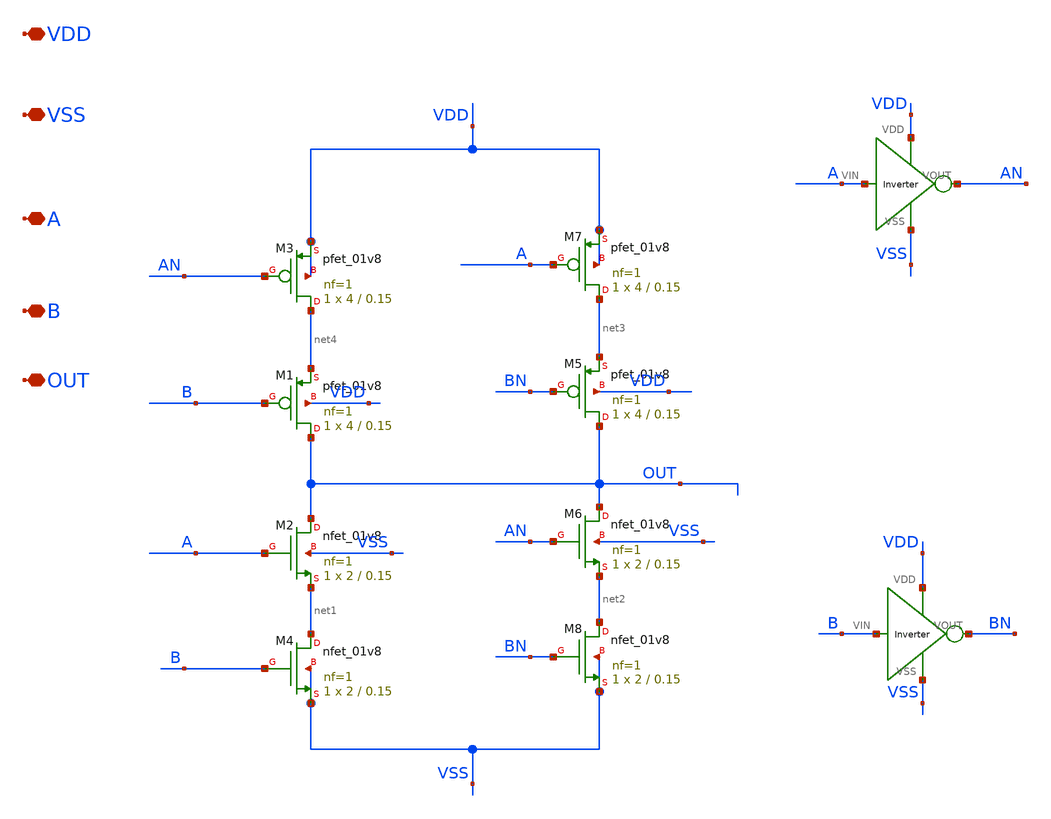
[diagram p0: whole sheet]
** sch_path: xschem/DC_DC_Converter_xschem/OTHERS/DC_DC_Converter_JV9/Delay_block_revised/XOR_for_symbol.sch
**.subckt XOR_for_symbol VDD VSS A B OUT
*.iopin VDD
*.iopin VSS
*.iopin A
*.iopin B
*.iopin OUT
XM1 OUT B net4 VDD sky130_fd_pr__pfet_01v8 L=0.15 W=4 nf=1 ad='int((nf+1)/2) * W/nf * 0.29' as='int((nf+2)/2) * W/nf * 0.29'
+ pd='2*int((nf+1)/2) * (W/nf + 0.29)' ps='2*int((nf+2)/2) * (W/nf + 0.29)' nrd='0.29 / W' nrs='0.29 / W'
+ sa=0 sb=0 sd=0 mult=1 m=1
XM2 OUT A net1 VSS sky130_fd_pr__nfet_01v8 L=0.15 W=2 nf=1 ad='int((nf+1)/2) * W/nf * 0.29' as='int((nf+2)/2) * W/nf * 0.29'
+ pd='2*int((nf+1)/2) * (W/nf + 0.29)' ps='2*int((nf+2)/2) * (W/nf + 0.29)' nrd='0.29 / W' nrs='0.29 / W'
+ sa=0 sb=0 sd=0 mult=1 m=1
XM3 net4 AN VDD VDD sky130_fd_pr__pfet_01v8 L=0.15 W=4 nf=1 ad='int((nf+1)/2) * W/nf * 0.29' as='int((nf+2)/2) * W/nf * 0.29'
+ pd='2*int((nf+1)/2) * (W/nf + 0.29)' ps='2*int((nf+2)/2) * (W/nf + 0.29)' nrd='0.29 / W' nrs='0.29 / W'
+ sa=0 sb=0 sd=0 mult=1 m=1
XM4 net1 B VSS VSS sky130_fd_pr__nfet_01v8 L=0.15 W=2 nf=1 ad='int((nf+1)/2) * W/nf * 0.29' as='int((nf+2)/2) * W/nf * 0.29'
+ pd='2*int((nf+1)/2) * (W/nf + 0.29)' ps='2*int((nf+2)/2) * (W/nf + 0.29)' nrd='0.29 / W' nrs='0.29 / W'
+ sa=0 sb=0 sd=0 mult=1 m=1
XM5 OUT BN net3 VDD sky130_fd_pr__pfet_01v8 L=0.15 W=4 nf=1 ad='int((nf+1)/2) * W/nf * 0.29' as='int((nf+2)/2) * W/nf * 0.29'
+ pd='2*int((nf+1)/2) * (W/nf + 0.29)' ps='2*int((nf+2)/2) * (W/nf + 0.29)' nrd='0.29 / W' nrs='0.29 / W'
+ sa=0 sb=0 sd=0 mult=1 m=1
XM6 OUT AN net2 VSS sky130_fd_pr__nfet_01v8 L=0.15 W=2 nf=1 ad='int((nf+1)/2) * W/nf * 0.29' as='int((nf+2)/2) * W/nf * 0.29'
+ pd='2*int((nf+1)/2) * (W/nf + 0.29)' ps='2*int((nf+2)/2) * (W/nf + 0.29)' nrd='0.29 / W' nrs='0.29 / W'
+ sa=0 sb=0 sd=0 mult=1 m=1
XM7 net3 A VDD VDD sky130_fd_pr__pfet_01v8 L=0.15 W=4 nf=1 ad='int((nf+1)/2) * W/nf * 0.29' as='int((nf+2)/2) * W/nf * 0.29'
+ pd='2*int((nf+1)/2) * (W/nf + 0.29)' ps='2*int((nf+2)/2) * (W/nf + 0.29)' nrd='0.29 / W' nrs='0.29 / W'
+ sa=0 sb=0 sd=0 mult=1 m=1
XM8 net2 BN VSS VSS sky130_fd_pr__nfet_01v8 L=0.15 W=2 nf=1 ad='int((nf+1)/2) * W/nf * 0.29' as='int((nf+2)/2) * W/nf * 0.29'
+ pd='2*int((nf+1)/2) * (W/nf + 0.29)' ps='2*int((nf+2)/2) * (W/nf + 0.29)' nrd='0.29 / W' nrs='0.29 / W'
+ sa=0 sb=0 sd=0 mult=1 m=1
X10 VSS VDD A AN Inverter
X1 VSS VDD B BN Inverter
**.ends

* expanding   symbol:  DC_DC_Converter/Inverter/Inverter.sym # of pins=4
** sym_path: DC_DC_Converter/Inverter/Inverter.sym
** sch_path: DC_DC_Converter/Inverter/Inverter.sch
.subckt Inverter VSS VDD VIN VOUT
*.ipin VIN
*.iopin VDD
*.iopin VSS
*.opin VOUT
XM1 VOUT VIN VSS VSS sky130_fd_pr__nfet_01v8 L=0.15 W=1 nf=1 ad='int((nf+1)/2) * W/nf * 0.29' as='int((nf+2)/2) * W/nf * 0.29'
+ pd='2*int((nf+1)/2) * (W/nf + 0.29)' ps='2*int((nf+2)/2) * (W/nf + 0.29)' nrd='0.29 / W' nrs='0.29 / W'
+ sa=0 sb=0 sd=0 mult=1 m=1
XM2 VOUT VIN VDD VDD sky130_fd_pr__pfet_01v8 L=0.15 W=2 nf=1 ad='int((nf+1)/2) * W/nf * 0.29' as='int((nf+2)/2) * W/nf * 0.29'
+ pd='2*int((nf+1)/2) * (W/nf + 0.29)' ps='2*int((nf+2)/2) * (W/nf + 0.29)' nrd='0.29 / W' nrs='0.29 / W'
+ sa=0 sb=0 sd=0 mult=1 m=1
.ends

.end
